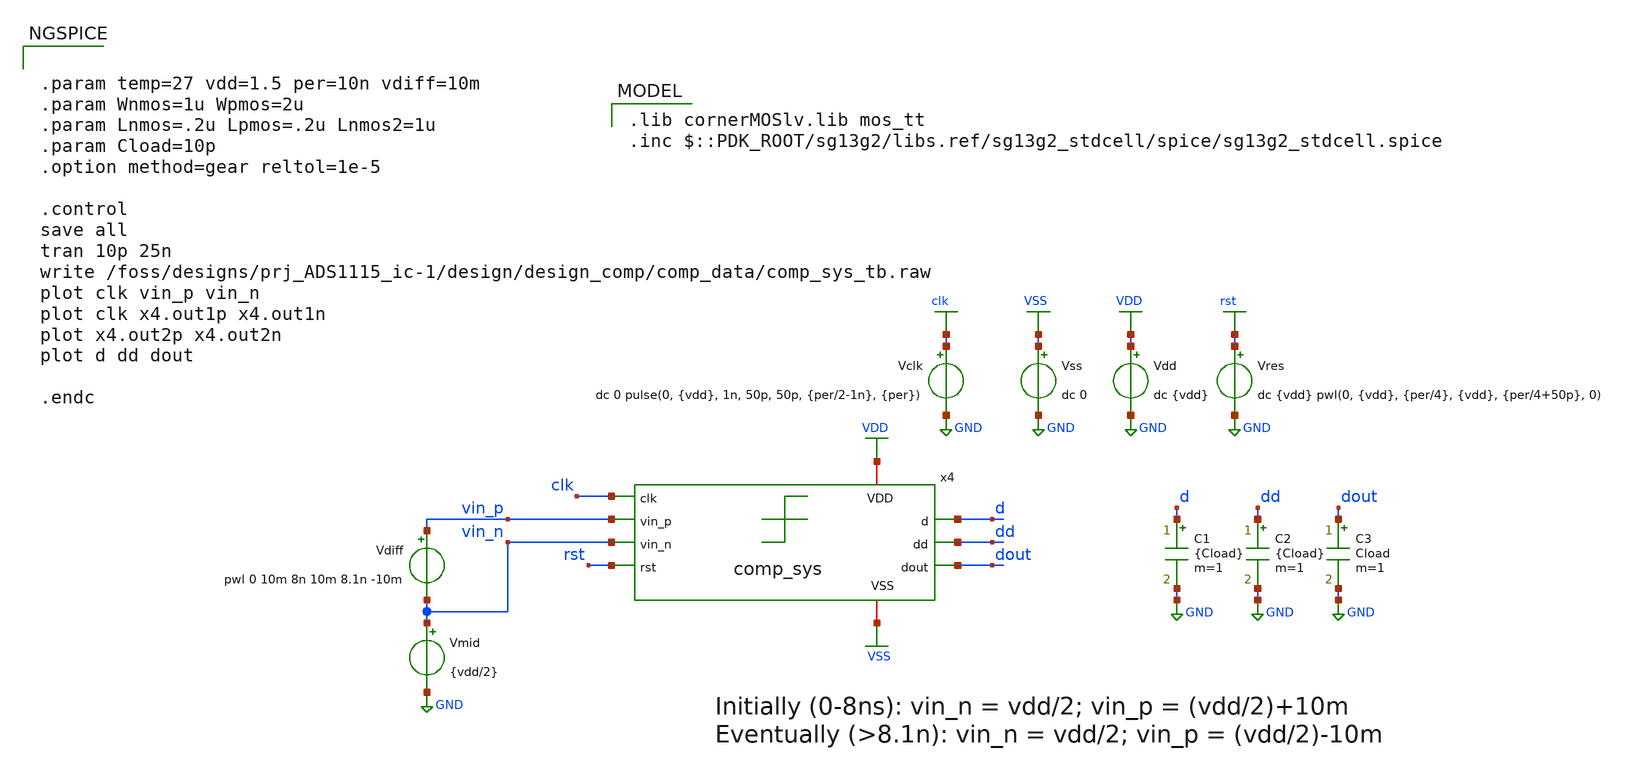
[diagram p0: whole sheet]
** sch_path: design/design_comp/tb_comp_sys_tran.sch
**.subckt tb_comp_sys_tran
Vdd VDD GND dc {vdd}
Vss VSS GND dc 0
Vdiff vin_p vin_n pwl 0 10m 8n 10m 8.1n -10m
Vmid vin_n GND {vdd/2}
Vclk clk GND dc 0 pulse(0, {vdd}, 1n, 50p, 50p, {per/2-1n}, {per})
Vres rst GND dc {vdd} pwl(0, {vdd}, {per/4}, {vdd}, {per/4+50p}, 0)
x4 VDD clk d vin_p vin_n dd rst dout VSS comp_sys
C1 d GND {Cload} m=1
C2 dd GND {Cload} m=1
C3 dout GND Cload m=1
**** begin user architecture code


.param temp=27 vdd=1.5 per=10n vdiff=10m
.param Wnmos=1u Wpmos=2u
.param Lnmos=.2u Lpmos=.2u Lnmos2=1u
.param Cload=10p
.option method=gear reltol=1e-5

.control
save all
tran 10p 25n
write /foss/designs/prj_ADS1115_ic-1/design/design_comp/comp_data/comp_sys_tb.raw
plot clk vin_p vin_n
plot clk x4.out1p x4.out1n
plot x4.out2p x4.out2n
plot d dd dout

.endc

 .lib cornerMOSlv.lib mos_tt
.inc $::PDK_ROOT/sg13g2/libs.ref/sg13g2_stdcell/spice/sg13g2_stdcell.spice
**** end user architecture code
**.ends
.GLOBAL GND
.GLOBAL VDD
.GLOBAL VSS
.GLOBAL clk
.GLOBAL rst
.end
